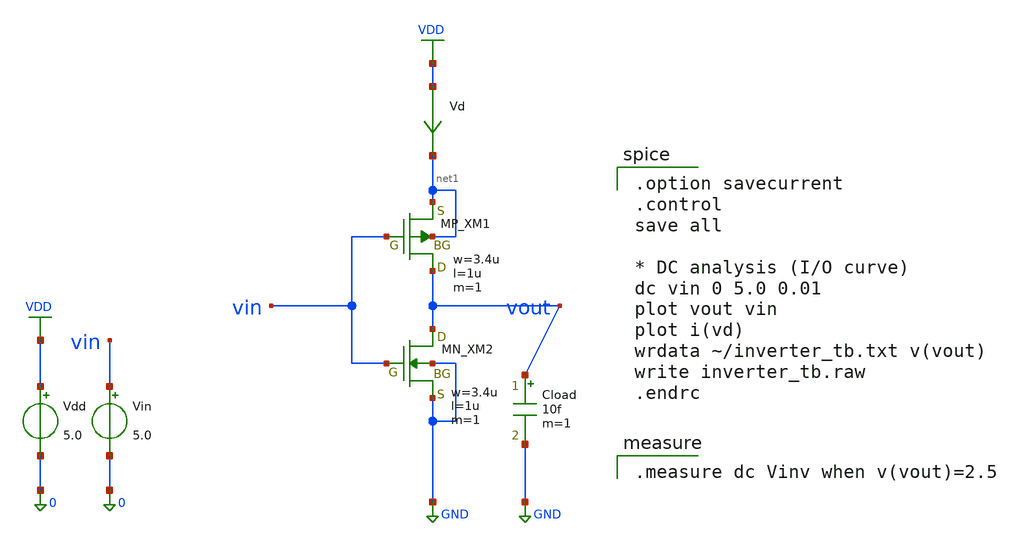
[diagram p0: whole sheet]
** sch_path: inverter-simulation.sch
**.subckt inverter-simulation
XXM1 vout vin net1 net1 PMOS w=3.4u l=1u nrd=0 nrs=0 m=1
XXM2 vout vin GND GND NMOS w=3.4u l=1u nrd=0 nrs=0 m=1
Vin vin 0 5.0
Vdd VDD 0 5.0
Vd VDD net1 0
.save i(vd)
Cload vout GND 10f m=1
**** begin user architecture code
 .include $::LIB/ip62_models

.option savecurrent
.control
save all

* DC analysis (I/O curve)
dc vin 0 5.0 0.01
plot vout vin
plot i(vd)
wrdata ~/inverter_tb.txt v(vout)
write inverter_tb.raw
.endrc


.measure dc Vinv when v(vout)=2.5

**** end user architecture code
**.ends
.GLOBAL VDD
.GLOBAL GND
.end
